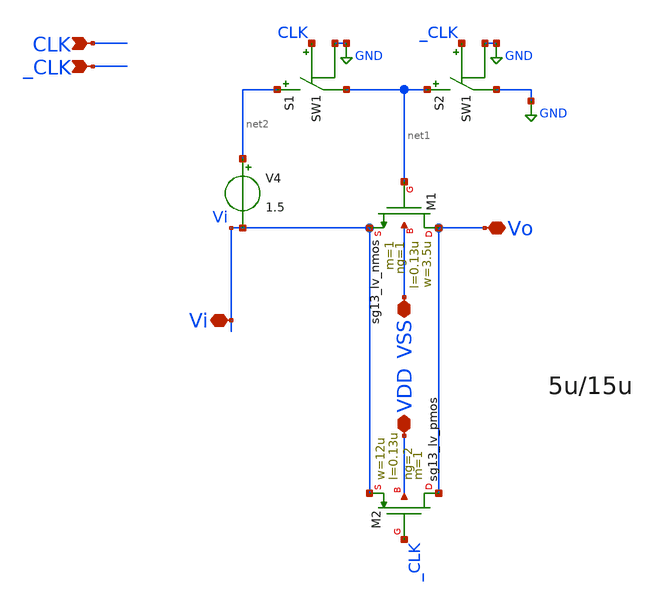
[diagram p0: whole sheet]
** sch_path: sch/blocks/sw_boost.sch
**.subckt sw_boost VSS CLK _CLK Vi Vo VDD
*.iopin VSS
*.ipin CLK
*.ipin _CLK
*.iopin Vi
*.iopin Vo
*.iopin VDD
XM1 Vo net1 Vi VSS sg13_lv_nmos w=3.5u l=0.13u ng=1 m=1 mm_ok=1
V4 net2 Vi 1.5
XM2 Vo _CLK Vi VDD sg13_lv_pmos w=12u l=0.13u ng=2 m=1 mm_ok=1
S1 net2 net1 CLK GND SW1
S2 net1 GND _CLK GND SW1
**.ends
.GLOBAL GND
**** begin user architecture code
.MODEL SW1 SW   VT=0.9 VH=0.01  RON=0.01 ROFF=10G
**** end user architecture code
.end
